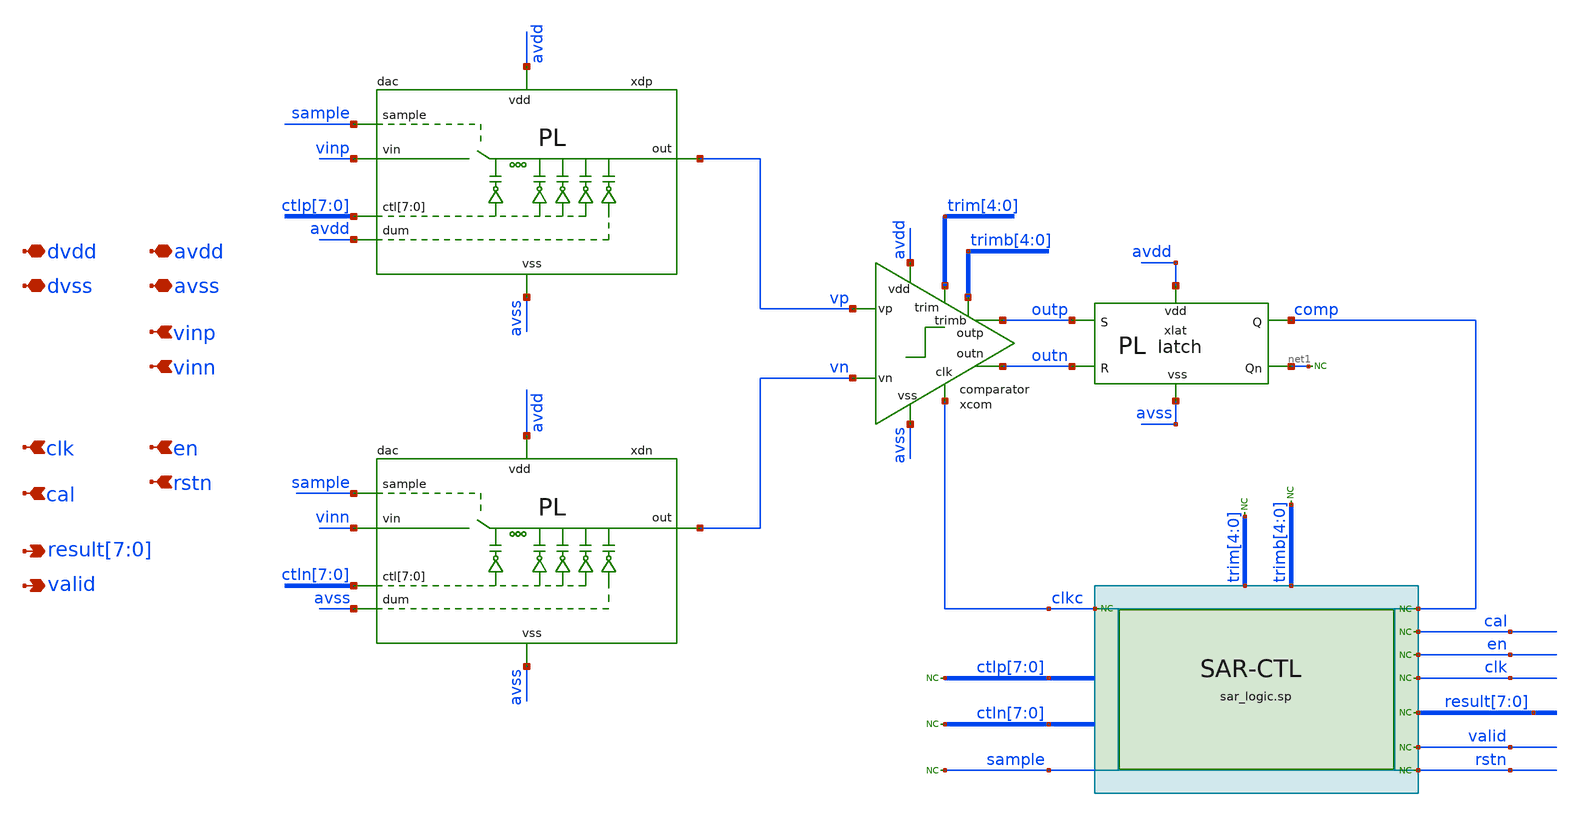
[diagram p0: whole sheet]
** sch_path: xschem/sar/sar/sar_with_digital.sch
**.subckt sar_with_digital avss avdd dvss dvdd vinp vinn
*+ result[7],result[6],result[5],result[4],result[3],result[2],result[1],result[0] clk en valid cal rstn
*.iopin avss
*.iopin avdd
*.iopin dvss
*.iopin dvdd
*.ipin vinp
*.ipin vinn
*.opin result[7],result[6],result[5],result[4],result[3],result[2],result[1],result[0]
*.ipin clk
*.ipin en
*.opin valid
*.ipin cal
*.ipin rstn
xlat avdd avss net1 outp outn comp latch
* noconn #net1
* noconn comp
* noconn sample
* noconn ctln[7:0]
* noconn ctlp[7:0]
* noconn trim[4:0]
* noconn trimb[4:0]
* noconn result[7:0]
* noconn valid
* noconn clkc
* noconn clk
* noconn en
* noconn cal
xdn vn sample avdd avss vinn ctln[7] ctln[6] ctln[5] ctln[4] ctln[3] ctln[2] ctln[1] ctln[0] avss
+ dac
xdp vp sample avdd avss vinp ctlp[7] ctlp[6] ctlp[5] ctlp[4] ctlp[3] ctlp[2] ctlp[1] ctlp[0] avdd
+ dac
xcom avss avdd clkc outp vp outn vn trim[4] trim[3] trim[2] trim[1] trim[0] trimb[4] trimb[3]
+ trimb[2] trimb[1] trimb[0] comparator
* noconn rstn
**** begin user architecture code

*.include $::DESIGN_PATH/sar/control/cmos_cells_digital.sp
*.include $::DESIGN_PATH/sar/control/sar_logic.sp
.include $::DESIGN_PATH/sar/sar_logic.spice



*.model adc_buff adc_bridge(in_low = 0.2 in_high=0.8)
*.model dac_buff dac_bridge(out_high = 1.2)

*Aad [clk rstn en comp cal] [dclk drstn den dcomp dcal] adc_buff
*Ada [dctlp0 dctlp1 dctlp2 dctlp3 dctlp4 dctlp5 dctlp6 dctlp7 dctln0 dctln1 dctln2 dctln3 dctln4
*+ dctln5 dctln6 dctln7 dres0 dres1 dres2 dres3 dres4 dres5 dres6 dres7 dsamp dclkc] [ctlp_0_ ctlp_1_ ctlp_2_
*+ ctlp_3_ ctlp_4_ ctlp_5_ ctlp_6_ ctlp_7_ ctln_0_ ctln_1_ ctln_2_ ctln_3_ ctln_4_ ctln_5_ ctln_6_ ctln_7_
*+ res0 res1 res2 res3 res4 res5 res6 res7 sample clkc] dac_buff
*Ada2 [dtrim4 dtrim3 dtrim2 dtrim1 dtrim0 dtrimb4 dtrimb3 dtrimb2 dtrimb1 dtrimb0] [trim_4_ trim_3_
*+ trim_2_ trim_1_ trim_0_ trimb_4_ trimb_3_ trimb_2_ trimb_1_ trimb_0_ ] dac_buff
*Xuut dvss dvdd dcal dclk dclkc dcomp dctln0 dctln1 dctln2 dctln3 dctln4 dctln5 dctln6 dctln7 dctlp0
*+ dctlp1 dctlp2 dctlp3 dctlp4 dctlp5 dctlp6 dctlp7 den dres0 dres1 dres2 dres3 dres4 dres5 dres6 dres7 drstn
*+ dsamp dtrim0 dtrim1 dtrim2 dtrim3 dtrim4 dtrimb0 dtrimb1 dtrimb2 dtrimb3 dtrimb4 dvalid sar_logic

Xuut dvss dvdd cal clk clkc comp ctln_0_ ctln_1_ ctln_2_ ctln_3_ ctln_4_ ctln_5_ ctln_6_ ctln_7_
+ ctlp_0_ ctlp_1_ ctlp_2_ ctlp_3_ ctlp_4_ ctlp_5_ ctlp_6_ ctlp_7_ en res0 res1 res2 res3 res4 res5 res6 res7
+ rstn sample trim_0 trim_1_ trim_2_ trim_3_ trim_4_ trimb_0_ trimb_1_ trimb_2_ trimb_3_ trimb_4_ dvalid
+ sar_logic



**** end user architecture code
**.ends

* expanding   symbol:  sar/comparator/comparator.sym # of pins=9
** sym_path: sar/comparator/comparator.sym
** sch_path: sar/comparator/comparator.sch
.subckt comparator vss vdd clk outp vp outn vn trim[4] trim[3] trim[2] trim[1] trim[0] trimb[4]
+ trimb[3] trimb[2] trimb[1] trimb[0]
*.ipin vn
*.ipin vp
*.ipin clk
*.iopin vdd
*.iopin vss
*.opin outp
*.opin outn
*.ipin trim[4],trim[3],trim[2],trim[1],trim[0]
*.ipin trimb[4],trimb[3],trimb[2],trimb[1],trimb[0]
x2 in trim[4] trim[3] trim[2] trim[1] trim[0] vss trim
x3 ip trimb[4] trimb[3] trimb[2] trimb[1] trimb[0] vss trim
XM1 in clk vdd vdd sky130_fd_pr__pfet_01v8 L=0.3 W=1 nf=1 ad='int((nf+1)/2) * W/nf * 0.29' as='int((nf+2)/2) * W/nf * 0.29'
+ pd='2*int((nf+1)/2) * (W/nf + 0.29)' ps='2*int((nf+2)/2) * (W/nf + 0.29)' nrd='0.29 / W' nrs='0.29 / W'
+ sa=0 sb=0 sd=0 mult=1 m=1
XM2 outn clk vdd vdd sky130_fd_pr__pfet_01v8 L=0.3 W=1 nf=1 ad='int((nf+1)/2) * W/nf * 0.29' as='int((nf+2)/2) * W/nf * 0.29'
+ pd='2*int((nf+1)/2) * (W/nf + 0.29)' ps='2*int((nf+2)/2) * (W/nf + 0.29)' nrd='0.29 / W' nrs='0.29 / W'
+ sa=0 sb=0 sd=0 mult=1 m=1
XM5 outn outp vdd vdd sky130_fd_pr__pfet_01v8 L=0.3 W=1 nf=1 ad='int((nf+1)/2) * W/nf * 0.29' as='int((nf+2)/2) * W/nf * 0.29'
+ pd='2*int((nf+1)/2) * (W/nf + 0.29)' ps='2*int((nf+2)/2) * (W/nf + 0.29)' nrd='0.29 / W' nrs='0.29 / W'
+ sa=0 sb=0 sd=0 mult=1 m=1
XMl4 outp outn vdd vdd sky130_fd_pr__pfet_01v8 L=0.3 W=1 nf=1 ad='int((nf+1)/2) * W/nf * 0.29' as='int((nf+2)/2) * W/nf * 0.29'
+ pd='2*int((nf+1)/2) * (W/nf + 0.29)' ps='2*int((nf+2)/2) * (W/nf + 0.29)' nrd='0.29 / W' nrs='0.29 / W'
+ sa=0 sb=0 sd=0 mult=1 m=1
XM3 outp clk vdd vdd sky130_fd_pr__pfet_01v8 L=0.3 W=1 nf=1 ad='int((nf+1)/2) * W/nf * 0.29' as='int((nf+2)/2) * W/nf * 0.29'
+ pd='2*int((nf+1)/2) * (W/nf + 0.29)' ps='2*int((nf+2)/2) * (W/nf + 0.29)' nrd='0.29 / W' nrs='0.29 / W'
+ sa=0 sb=0 sd=0 mult=1 m=1
XM4 ip clk vdd vdd sky130_fd_pr__pfet_01v8 L=0.3 W=1 nf=1 ad='int((nf+1)/2) * W/nf * 0.29' as='int((nf+2)/2) * W/nf * 0.29'
+ pd='2*int((nf+1)/2) * (W/nf + 0.29)' ps='2*int((nf+2)/2) * (W/nf + 0.29)' nrd='0.29 / W' nrs='0.29 / W'
+ sa=0 sb=0 sd=0 mult=1 m=1
XMl2 outp outn ip vss sky130_fd_pr__nfet_01v8 L=0.3 W=1 nf=1 ad='int((nf+1)/2) * W/nf * 0.29' as='int((nf+2)/2) * W/nf * 0.29'
+ pd='2*int((nf+1)/2) * (W/nf + 0.29)' ps='2*int((nf+2)/2) * (W/nf + 0.29)' nrd='0.29 / W' nrs='0.29 / W'
+ sa=0 sb=0 sd=0 mult=1 m=1
XMl1 outn outp in vss sky130_fd_pr__nfet_01v8 L=0.3 W=1 nf=1 ad='int((nf+1)/2) * W/nf * 0.29' as='int((nf+2)/2) * W/nf * 0.29'
+ pd='2*int((nf+1)/2) * (W/nf + 0.29)' ps='2*int((nf+2)/2) * (W/nf + 0.29)' nrd='0.29 / W' nrs='0.29 / W'
+ sa=0 sb=0 sd=0 mult=1 m=1
XMinn in vn diff vss sky130_fd_pr__nfet_01v8 L=0.3 W=1 nf=1 ad='int((nf+1)/2) * W/nf * 0.29' as='int((nf+2)/2) * W/nf * 0.29'
+ pd='2*int((nf+1)/2) * (W/nf + 0.29)' ps='2*int((nf+2)/2) * (W/nf + 0.29)' nrd='0.29 / W' nrs='0.29 / W'
+ sa=0 sb=0 sd=0 mult=1 m=1
XMinp ip vp diff vss sky130_fd_pr__nfet_01v8 L=0.3 W=1 nf=1 ad='int((nf+1)/2) * W/nf * 0.29' as='int((nf+2)/2) * W/nf * 0.29'
+ pd='2*int((nf+1)/2) * (W/nf + 0.29)' ps='2*int((nf+2)/2) * (W/nf + 0.29)' nrd='0.29 / W' nrs='0.29 / W'
+ sa=0 sb=0 sd=0 mult=1 m=1
XMdiff diff clk vss vss sky130_fd_pr__nfet_01v8 L=0.3 W=1 nf=1 ad='int((nf+1)/2) * W/nf * 0.29' as='int((nf+2)/2) * W/nf * 0.29'
+ pd='2*int((nf+1)/2) * (W/nf + 0.29)' ps='2*int((nf+2)/2) * (W/nf + 0.29)' nrd='0.29 / W' nrs='0.29 / W'
+ sa=0 sb=0 sd=0 mult=2 m=2
.ends


* expanding   symbol:  sar/comparator/trim.sym # of pins=3
** sym_path: sar/comparator/trim.sym
** sch_path: sar/comparator/trim.sch
.subckt trim drain d[4] d[3] d[2] d[1] d[0] vss
*.iopin vss
*.ipin d[4],d[3],d[2],d[1],d[0]
*.opin drain
x4[7] drain n4 trimcap
x4[6] drain n4 trimcap
x4[5] drain n4 trimcap
x4[4] drain n4 trimcap
x4[3] drain n4 trimcap
x4[2] drain n4 trimcap
x4[1] drain n4 trimcap
x4[0] drain n4 trimcap
x3[3] drain n3 trimcap
x3[2] drain n3 trimcap
x3[1] drain n3 trimcap
x3[0] drain n3 trimcap
x2[1] drain n2 trimcap
x2[0] drain n2 trimcap
x1 drain n1 trimcap
x0 drain n0 trimcap
XM4[7] n4 d[4] vss vss sky130_fd_pr__nfet_01v8_lvt L=0.3 W=1 nf=1 ad='int((nf+1)/2) * W/nf * 0.29' as='int((nf+2)/2) * W/nf * 0.29'
+ pd='2*int((nf+1)/2) * (W/nf + 0.29)' ps='2*int((nf+2)/2) * (W/nf + 0.29)' nrd='0.29 / W' nrs='0.29 / W'
+ sa=0 sb=0 sd=0 mult=1 m=1
XM4[6] n4 d[4] vss vss sky130_fd_pr__nfet_01v8_lvt L=0.3 W=1 nf=1 ad='int((nf+1)/2) * W/nf * 0.29' as='int((nf+2)/2) * W/nf * 0.29'
+ pd='2*int((nf+1)/2) * (W/nf + 0.29)' ps='2*int((nf+2)/2) * (W/nf + 0.29)' nrd='0.29 / W' nrs='0.29 / W'
+ sa=0 sb=0 sd=0 mult=1 m=1
XM4[5] n4 d[4] vss vss sky130_fd_pr__nfet_01v8_lvt L=0.3 W=1 nf=1 ad='int((nf+1)/2) * W/nf * 0.29' as='int((nf+2)/2) * W/nf * 0.29'
+ pd='2*int((nf+1)/2) * (W/nf + 0.29)' ps='2*int((nf+2)/2) * (W/nf + 0.29)' nrd='0.29 / W' nrs='0.29 / W'
+ sa=0 sb=0 sd=0 mult=1 m=1
XM4[4] n4 d[4] vss vss sky130_fd_pr__nfet_01v8_lvt L=0.3 W=1 nf=1 ad='int((nf+1)/2) * W/nf * 0.29' as='int((nf+2)/2) * W/nf * 0.29'
+ pd='2*int((nf+1)/2) * (W/nf + 0.29)' ps='2*int((nf+2)/2) * (W/nf + 0.29)' nrd='0.29 / W' nrs='0.29 / W'
+ sa=0 sb=0 sd=0 mult=1 m=1
XM4[3] n4 d[4] vss vss sky130_fd_pr__nfet_01v8_lvt L=0.3 W=1 nf=1 ad='int((nf+1)/2) * W/nf * 0.29' as='int((nf+2)/2) * W/nf * 0.29'
+ pd='2*int((nf+1)/2) * (W/nf + 0.29)' ps='2*int((nf+2)/2) * (W/nf + 0.29)' nrd='0.29 / W' nrs='0.29 / W'
+ sa=0 sb=0 sd=0 mult=1 m=1
XM4[2] n4 d[4] vss vss sky130_fd_pr__nfet_01v8_lvt L=0.3 W=1 nf=1 ad='int((nf+1)/2) * W/nf * 0.29' as='int((nf+2)/2) * W/nf * 0.29'
+ pd='2*int((nf+1)/2) * (W/nf + 0.29)' ps='2*int((nf+2)/2) * (W/nf + 0.29)' nrd='0.29 / W' nrs='0.29 / W'
+ sa=0 sb=0 sd=0 mult=1 m=1
XM4[1] n4 d[4] vss vss sky130_fd_pr__nfet_01v8_lvt L=0.3 W=1 nf=1 ad='int((nf+1)/2) * W/nf * 0.29' as='int((nf+2)/2) * W/nf * 0.29'
+ pd='2*int((nf+1)/2) * (W/nf + 0.29)' ps='2*int((nf+2)/2) * (W/nf + 0.29)' nrd='0.29 / W' nrs='0.29 / W'
+ sa=0 sb=0 sd=0 mult=1 m=1
XM4[0] n4 d[4] vss vss sky130_fd_pr__nfet_01v8_lvt L=0.3 W=1 nf=1 ad='int((nf+1)/2) * W/nf * 0.29' as='int((nf+2)/2) * W/nf * 0.29'
+ pd='2*int((nf+1)/2) * (W/nf + 0.29)' ps='2*int((nf+2)/2) * (W/nf + 0.29)' nrd='0.29 / W' nrs='0.29 / W'
+ sa=0 sb=0 sd=0 mult=1 m=1
XM3[3] n3 d[3] vss vss sky130_fd_pr__nfet_01v8_lvt L=0.3 W=1 nf=1 ad='int((nf+1)/2) * W/nf * 0.29' as='int((nf+2)/2) * W/nf * 0.29'
+ pd='2*int((nf+1)/2) * (W/nf + 0.29)' ps='2*int((nf+2)/2) * (W/nf + 0.29)' nrd='0.29 / W' nrs='0.29 / W'
+ sa=0 sb=0 sd=0 mult=1 m=1
XM3[2] n3 d[3] vss vss sky130_fd_pr__nfet_01v8_lvt L=0.3 W=1 nf=1 ad='int((nf+1)/2) * W/nf * 0.29' as='int((nf+2)/2) * W/nf * 0.29'
+ pd='2*int((nf+1)/2) * (W/nf + 0.29)' ps='2*int((nf+2)/2) * (W/nf + 0.29)' nrd='0.29 / W' nrs='0.29 / W'
+ sa=0 sb=0 sd=0 mult=1 m=1
XM3[1] n3 d[3] vss vss sky130_fd_pr__nfet_01v8_lvt L=0.3 W=1 nf=1 ad='int((nf+1)/2) * W/nf * 0.29' as='int((nf+2)/2) * W/nf * 0.29'
+ pd='2*int((nf+1)/2) * (W/nf + 0.29)' ps='2*int((nf+2)/2) * (W/nf + 0.29)' nrd='0.29 / W' nrs='0.29 / W'
+ sa=0 sb=0 sd=0 mult=1 m=1
XM3[0] n3 d[3] vss vss sky130_fd_pr__nfet_01v8_lvt L=0.3 W=1 nf=1 ad='int((nf+1)/2) * W/nf * 0.29' as='int((nf+2)/2) * W/nf * 0.29'
+ pd='2*int((nf+1)/2) * (W/nf + 0.29)' ps='2*int((nf+2)/2) * (W/nf + 0.29)' nrd='0.29 / W' nrs='0.29 / W'
+ sa=0 sb=0 sd=0 mult=1 m=1
XM2[1] n2 d[2] vss vss sky130_fd_pr__nfet_01v8_lvt L=0.3 W=1 nf=1 ad='int((nf+1)/2) * W/nf * 0.29' as='int((nf+2)/2) * W/nf * 0.29'
+ pd='2*int((nf+1)/2) * (W/nf + 0.29)' ps='2*int((nf+2)/2) * (W/nf + 0.29)' nrd='0.29 / W' nrs='0.29 / W'
+ sa=0 sb=0 sd=0 mult=1 m=1
XM2[0] n2 d[2] vss vss sky130_fd_pr__nfet_01v8_lvt L=0.3 W=1 nf=1 ad='int((nf+1)/2) * W/nf * 0.29' as='int((nf+2)/2) * W/nf * 0.29'
+ pd='2*int((nf+1)/2) * (W/nf + 0.29)' ps='2*int((nf+2)/2) * (W/nf + 0.29)' nrd='0.29 / W' nrs='0.29 / W'
+ sa=0 sb=0 sd=0 mult=1 m=1
XM1 n1 d[1] vss vss sky130_fd_pr__nfet_01v8_lvt L=0.3 W=1 nf=1 ad='int((nf+1)/2) * W/nf * 0.29' as='int((nf+2)/2) * W/nf * 0.29'
+ pd='2*int((nf+1)/2) * (W/nf + 0.29)' ps='2*int((nf+2)/2) * (W/nf + 0.29)' nrd='0.29 / W' nrs='0.29 / W'
+ sa=0 sb=0 sd=0 mult=1 m=1
XM2 n0 d[0] vss vss sky130_fd_pr__nfet_01v8_lvt L=0.3 W=1 nf=1 ad='int((nf+1)/2) * W/nf * 0.29' as='int((nf+2)/2) * W/nf * 0.29'
+ pd='2*int((nf+1)/2) * (W/nf + 0.29)' ps='2*int((nf+2)/2) * (W/nf + 0.29)' nrd='0.29 / W' nrs='0.29 / W'
+ sa=0 sb=0 sd=0 mult=1 m=1
.ends


* expanding   symbol:  sar/comparator/trimcap.sym # of pins=2
** sym_path: sar/comparator/trimcap.sym
** sch_path: sar/comparator/trimcap.sch
.subckt trimcap cp cn
*.iopin cp
*.iopin cn
XC2 cp cn sky130_fd_pr__cap_mim_m3_1 W=1 L=1 MF=1 m=1
.ends

.end
